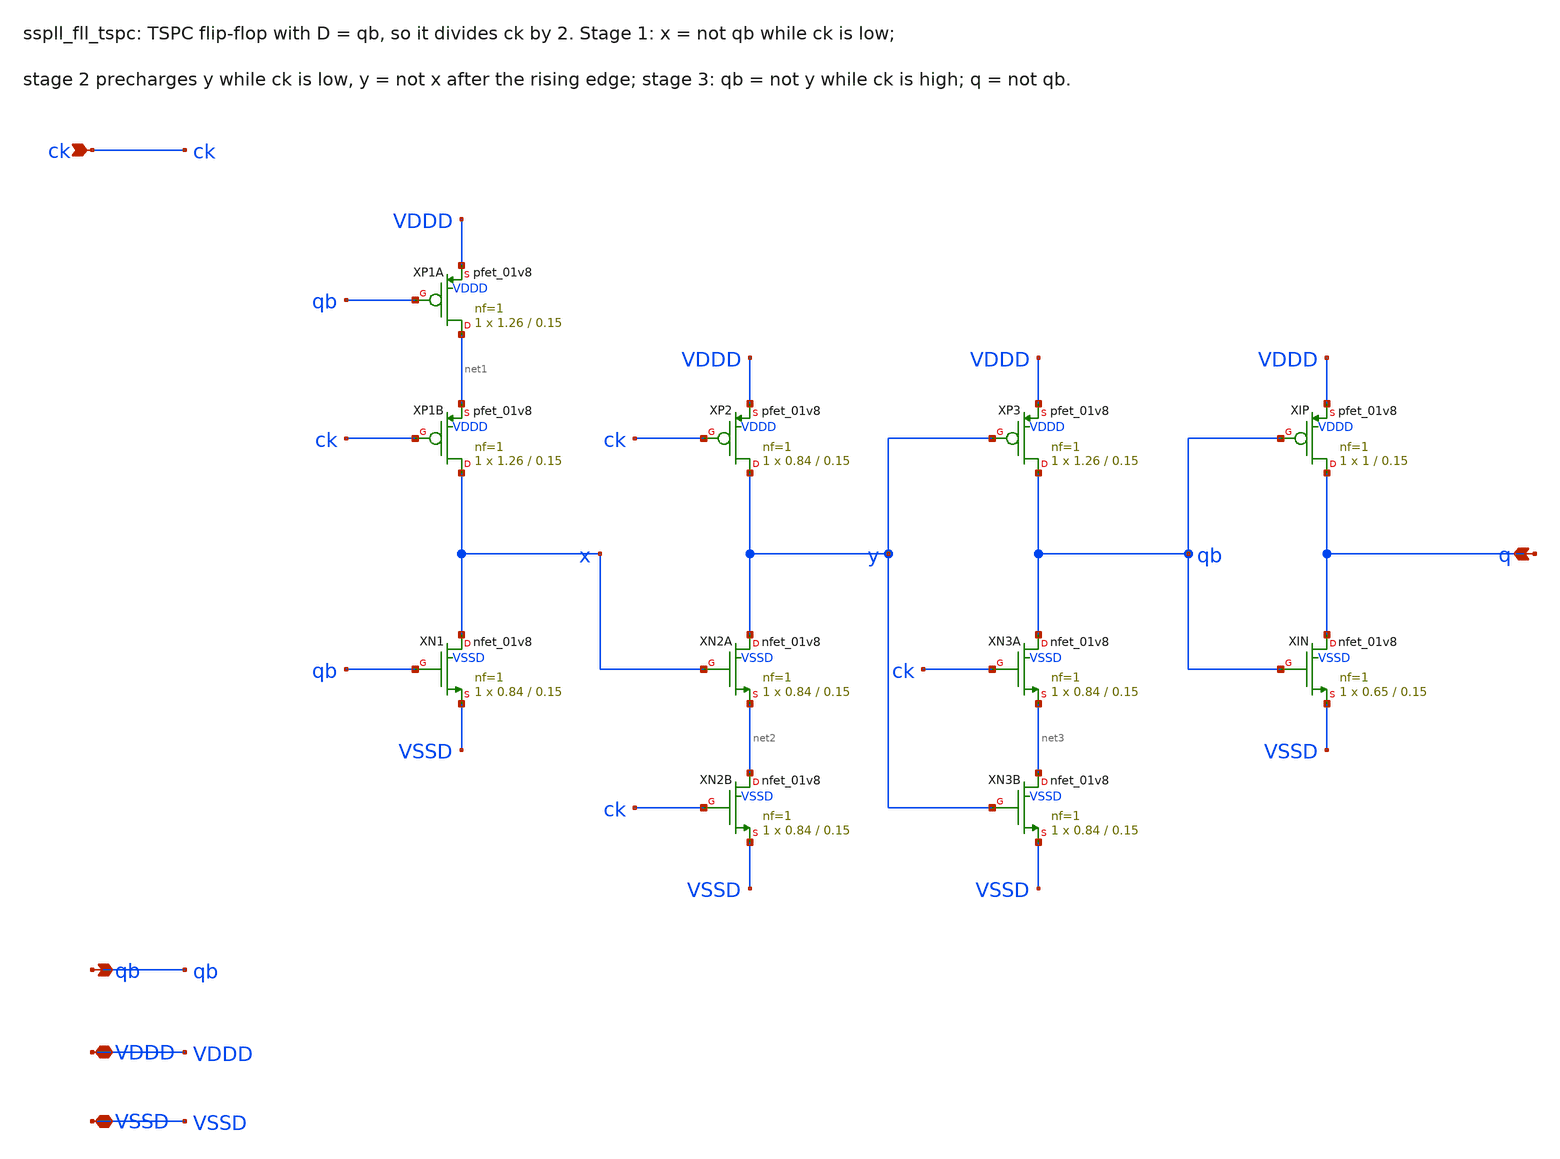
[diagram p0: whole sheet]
** sch_path: xschem/fll_hv/sspll_fll_tspc.sch
**.subckt sspll_fll_tspc q qb ck VDDD VSSD
*.opin q
*.opin qb
*.ipin ck
*.iopin VDDD
*.iopin VSSD
XXP1A net1 qb VDDD VDDD sky130_fd_pr__pfet_01v8 L=0.15 W=1.26 nf=1 ad='int((nf+1)/2) * W/nf * 0.29' as='int((nf+2)/2) * W/nf * 0.29'
+ pd='2*int((nf+1)/2) * (W/nf + 0.29)' ps='2*int((nf+2)/2) * (W/nf + 0.29)' nrd='0.29 / W' nrs='0.29 / W'
+ sa=0 sb=0 sd=0 mult=1 m=1
XXP1B x ck net1 VDDD sky130_fd_pr__pfet_01v8 L=0.15 W=1.26 nf=1 ad='int((nf+1)/2) * W/nf * 0.29' as='int((nf+2)/2) * W/nf * 0.29'
+ pd='2*int((nf+1)/2) * (W/nf + 0.29)' ps='2*int((nf+2)/2) * (W/nf + 0.29)' nrd='0.29 / W' nrs='0.29 / W'
+ sa=0 sb=0 sd=0 mult=1 m=1
XXN1 x qb VSSD VSSD sky130_fd_pr__nfet_01v8 L=0.15 W=0.84 nf=1 ad='int((nf+1)/2) * W/nf * 0.29' as='int((nf+2)/2) * W/nf * 0.29'
+ pd='2*int((nf+1)/2) * (W/nf + 0.29)' ps='2*int((nf+2)/2) * (W/nf + 0.29)' nrd='0.29 / W' nrs='0.29 / W'
+ sa=0 sb=0 sd=0 mult=1 m=1
XXP2 y ck VDDD VDDD sky130_fd_pr__pfet_01v8 L=0.15 W=0.84 nf=1 ad='int((nf+1)/2) * W/nf * 0.29' as='int((nf+2)/2) * W/nf * 0.29'
+ pd='2*int((nf+1)/2) * (W/nf + 0.29)' ps='2*int((nf+2)/2) * (W/nf + 0.29)' nrd='0.29 / W' nrs='0.29 / W'
+ sa=0 sb=0 sd=0 mult=1 m=1
XXN2A y x net2 VSSD sky130_fd_pr__nfet_01v8 L=0.15 W=0.84 nf=1 ad='int((nf+1)/2) * W/nf * 0.29' as='int((nf+2)/2) * W/nf * 0.29'
+ pd='2*int((nf+1)/2) * (W/nf + 0.29)' ps='2*int((nf+2)/2) * (W/nf + 0.29)' nrd='0.29 / W' nrs='0.29 / W'
+ sa=0 sb=0 sd=0 mult=1 m=1
XXN2B net2 ck VSSD VSSD sky130_fd_pr__nfet_01v8 L=0.15 W=0.84 nf=1 ad='int((nf+1)/2) * W/nf * 0.29' as='int((nf+2)/2) * W/nf * 0.29'
+ pd='2*int((nf+1)/2) * (W/nf + 0.29)' ps='2*int((nf+2)/2) * (W/nf + 0.29)' nrd='0.29 / W' nrs='0.29 / W'
+ sa=0 sb=0 sd=0 mult=1 m=1
XXP3 qb y VDDD VDDD sky130_fd_pr__pfet_01v8 L=0.15 W=1.26 nf=1 ad='int((nf+1)/2) * W/nf * 0.29' as='int((nf+2)/2) * W/nf * 0.29'
+ pd='2*int((nf+1)/2) * (W/nf + 0.29)' ps='2*int((nf+2)/2) * (W/nf + 0.29)' nrd='0.29 / W' nrs='0.29 / W'
+ sa=0 sb=0 sd=0 mult=1 m=1
XXN3A qb ck net3 VSSD sky130_fd_pr__nfet_01v8 L=0.15 W=0.84 nf=1 ad='int((nf+1)/2) * W/nf * 0.29' as='int((nf+2)/2) * W/nf * 0.29'
+ pd='2*int((nf+1)/2) * (W/nf + 0.29)' ps='2*int((nf+2)/2) * (W/nf + 0.29)' nrd='0.29 / W' nrs='0.29 / W'
+ sa=0 sb=0 sd=0 mult=1 m=1
XXN3B net3 y VSSD VSSD sky130_fd_pr__nfet_01v8 L=0.15 W=0.84 nf=1 ad='int((nf+1)/2) * W/nf * 0.29' as='int((nf+2)/2) * W/nf * 0.29'
+ pd='2*int((nf+1)/2) * (W/nf + 0.29)' ps='2*int((nf+2)/2) * (W/nf + 0.29)' nrd='0.29 / W' nrs='0.29 / W'
+ sa=0 sb=0 sd=0 mult=1 m=1
XXIP q qb VDDD VDDD sky130_fd_pr__pfet_01v8 L=0.15 W=1 nf=1 ad='int((nf+1)/2) * W/nf * 0.29' as='int((nf+2)/2) * W/nf * 0.29'
+ pd='2*int((nf+1)/2) * (W/nf + 0.29)' ps='2*int((nf+2)/2) * (W/nf + 0.29)' nrd='0.29 / W' nrs='0.29 / W'
+ sa=0 sb=0 sd=0 mult=1 m=1
XXIN q qb VSSD VSSD sky130_fd_pr__nfet_01v8 L=0.15 W=0.65 nf=1 ad='int((nf+1)/2) * W/nf * 0.29' as='int((nf+2)/2) * W/nf * 0.29'
+ pd='2*int((nf+1)/2) * (W/nf + 0.29)' ps='2*int((nf+2)/2) * (W/nf + 0.29)' nrd='0.29 / W' nrs='0.29 / W'
+ sa=0 sb=0 sd=0 mult=1 m=1
**.ends
.end
